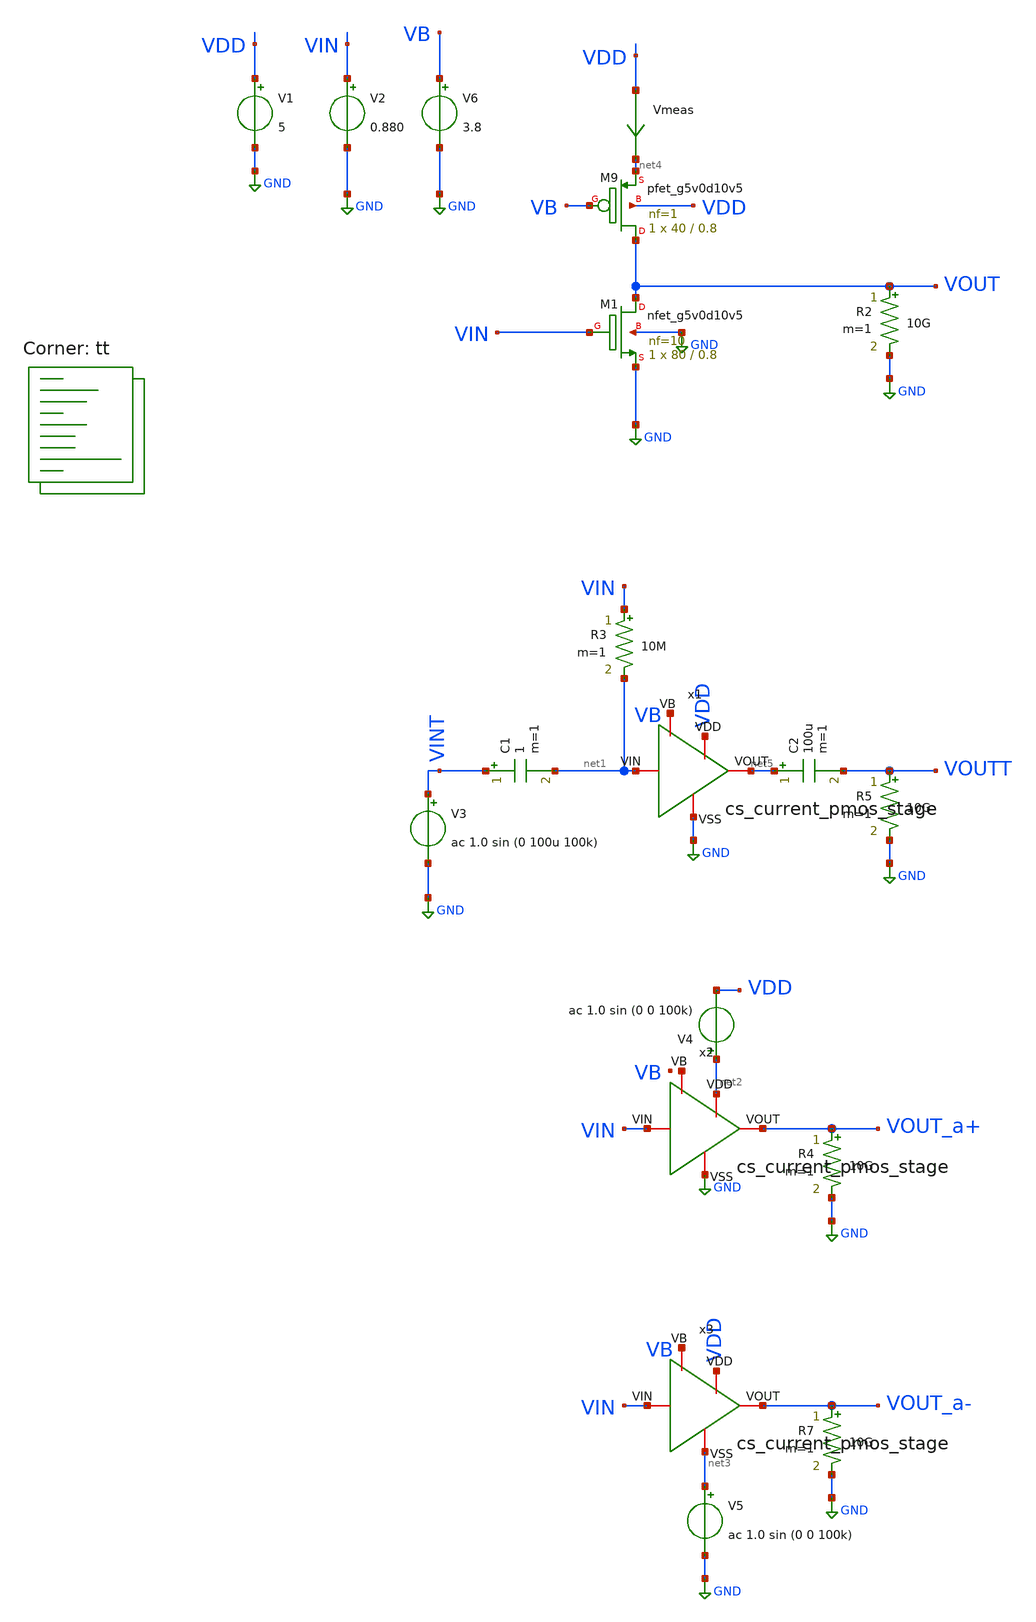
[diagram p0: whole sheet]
** sch_path: amplifiers/single_stage_amps/basic_stages/cs_current_pmos_stage/cs_current_pmos_stage_test.sch
**.subckt cs_current_pmos_stage_test
Vmeas VDD net4 0
.save i(vmeas)
V1 VDD GND 5
V2 VIN GND 0.880
V3 VINT GND ac 1.0 sin (0 100u 100k)
R2 VOUT GND 10G m=1
C1 VINT net1 1 m=1
R3 VIN net1 10M m=1
R5 VOUTT GND 10G m=1
C2 net5 VOUTT 100u m=1
R4 VOUT_a+ GND 10G m=1
V4 net2 VDD ac 1.0 sin (0 0 100k)
R7 VOUT_a- GND 10G m=1
V5 net3 GND ac 1.0 sin (0 0 100k)
XM1 VOUT VIN GND GND sky130_fd_pr__nfet_g5v0d10v5 L=0.8 W=80 nf=10 ad='int((10 + 1)/2) * 80 / 10 * 0.29'
+ as='int((10 + 2)/2) * 80 / 10 * 0.29' pd='2*int((10 + 1)/2) * (80 / 10 + 0.29)' ps='2*int((10 + 2)/2) * (80 / 10 + 0.29)'
+ nrd='0.29 / 80 ' nrs='0.29 / 80 ' sa=0 sb=0 sd=0 mult=1 m=1
XM9 VOUT VB net4 VDD sky130_fd_pr__pfet_g5v0d10v5 L=0.8 W=40 nf=1 ad='int((1 + 1)/2) * 40 / 1 * 0.29'
+ as='int((1 + 2)/2) * 40 / 1 * 0.29' pd='2*int((1 + 1)/2) * (40 / 1 + 0.29)' ps='2*int((1 + 2)/2) * (40 / 1 + 0.29)'
+ nrd='0.29 / 40 ' nrs='0.29 / 40 ' sa=0 sb=0 sd=0 mult=1 m=1
V6 VB GND 3.8
x1 VDD GND net1 net5 VB cs_current_pmos_stage
x2 net2 GND VIN VOUT_a+ net6 cs_current_pmos_stage
x3 VDD net3 VIN VOUT_a- VB cs_current_pmos_stage
**** begin user architecture code

**************************************************************
**************************************************************
**************************************************************
**************************************************************
**************************************************************
*LIBs*********************************************************
**************************************************************
**************************************************************
**************************************************************
**************************************************************
**************************************************************
*.lib $::SKYWATER_MODELS/sky130.lib.spice tt
* chose the corners in the corner file
* tt_mm for mismatch
* ss ff sf fs standart corners
* ll hh lh hl capacitor and resistors corners
* mc for total process variation including corners
**************************************************************
**************************************************************
**************************************************************
**************************************************************
**************************************************************
*Corners/montecarlo options***********************************
**************************************************************
**************************************************************
**************************************************************
**************************************************************
**************************************************************
.TEMP 27
**************************************************************
**************************************************************
**************************************************************
**************************************************************
*SIMULATION and Plots*****************************************
**************************************************************
**************************************************************
**************************************************************
**************************************************************
.control
save all
dc V2 0 5 0.01
*dc simulation
plot v(VOUT) v(VIN) deriv(v(VOUT))
*ploting VIN VOUT and the voltage gain
plot i(Vmeas)
*ploting the current for curiosity
tran 0.1ns 20u
*transient simulation
plot (v(VINT)) (v(VOUTT))
*simple plot to exemplify the gain
fft v(VOUTT) v(VINT)
*fast fourier transfor
plot mag(v(VOUTT)) mag(v(VINT))
* analyse the frequency spectrum of the transient waves, to detect distortion
ac dec 20 1 50G
*simple ac simulation
plot db(v(VOUTT))
plot db(v(VOUT_a+))
plot db(v(VOUT_a-))
*gain in function of the input frequency
.endc

.lib $::SKYWATER_MODELS/sky130.lib.spice tt

** Additional definitions for NPN
.param  dkisnpn1x1=8.7913e-01 dkbfnpn1x1=9.8501e-01  dkisnpn1x2=9.0950e-01 dkbfnpn1x2=9.6759e-01
+  dkisnpnpolyhv=1.0 dkbfnpnpolyhv=1.0


**** end user architecture code
**.ends
.GLOBAL GND
.end
